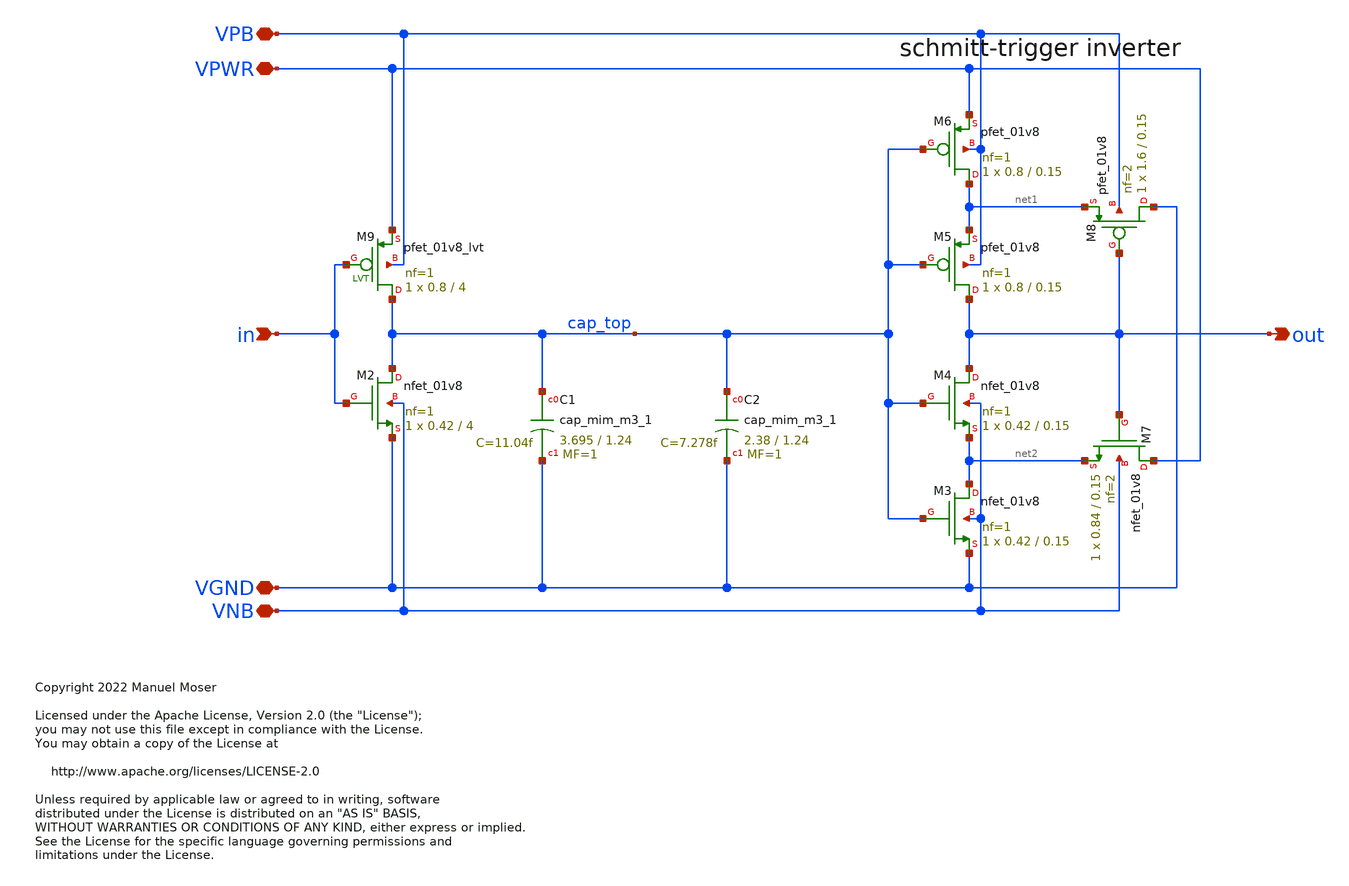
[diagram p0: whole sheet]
** sch_path: xschem/archive/sky130_mm_sc_hd_dlyMim5ns/sky130_mm_sc_hd_dlyMim5ns.sch
* Copyright 2022 Manuel Moser
* Licensed under the Apache License, Version 2.0 (the "License");
**.subckt sky130_mm_sc_hd_dlyMim5ns VPWR VGND in out VPB VNB
*.iopin VPWR
*.iopin VGND
*.ipin in
*.opin out
*.iopin VPB
*.iopin VNB
XM2 cap_top in VGND VNB sky130_fd_pr__nfet_01v8 L=4 W=0.42 nf=1 ad='int((nf+1)/2) * W/nf * 0.29' as='int((nf+2)/2) * W/nf * 0.29'
+ pd='2*int((nf+1)/2) * (W/nf + 0.29)' ps='2*int((nf+2)/2) * (W/nf + 0.29)' nrd='0.29 / W' nrs='0.29 / W'
+ sa=0 sb=0 sd=0 mult=1 m=1
XM3 net2 cap_top VGND VNB sky130_fd_pr__nfet_01v8 L=0.15 W=0.42 nf=1 ad='int((nf+1)/2) * W/nf * 0.29'
+ as='int((nf+2)/2) * W/nf * 0.29' pd='2*int((nf+1)/2) * (W/nf + 0.29)' ps='2*int((nf+2)/2) * (W/nf + 0.29)'
+ nrd='0.29 / W' nrs='0.29 / W' sa=0 sb=0 sd=0 mult=1 m=1
XM4 out cap_top net2 VNB sky130_fd_pr__nfet_01v8 L=0.15 W=0.42 nf=1 ad='int((nf+1)/2) * W/nf * 0.29'
+ as='int((nf+2)/2) * W/nf * 0.29' pd='2*int((nf+1)/2) * (W/nf + 0.29)' ps='2*int((nf+2)/2) * (W/nf + 0.29)'
+ nrd='0.29 / W' nrs='0.29 / W' sa=0 sb=0 sd=0 mult=1 m=1
XM5 out cap_top net1 VPB sky130_fd_pr__pfet_01v8 L=0.15 W=0.8 nf=1 ad='int((nf+1)/2) * W/nf * 0.29' as='int((nf+2)/2) * W/nf * 0.29'
+ pd='2*int((nf+1)/2) * (W/nf + 0.29)' ps='2*int((nf+2)/2) * (W/nf + 0.29)' nrd='0.29 / W' nrs='0.29 / W'
+ sa=0 sb=0 sd=0 mult=1 m=1
XM6 net1 cap_top VPWR VPB sky130_fd_pr__pfet_01v8 L=0.15 W=0.8 nf=1 ad='int((nf+1)/2) * W/nf * 0.29'
+ as='int((nf+2)/2) * W/nf * 0.29' pd='2*int((nf+1)/2) * (W/nf + 0.29)' ps='2*int((nf+2)/2) * (W/nf + 0.29)'
+ nrd='0.29 / W' nrs='0.29 / W' sa=0 sb=0 sd=0 mult=1 m=1
XM7 VPWR out net2 VNB sky130_fd_pr__nfet_01v8 L=0.15 W=0.84 nf=2 ad='int((nf+1)/2) * W/nf * 0.29' as='int((nf+2)/2) * W/nf * 0.29'
+ pd='2*int((nf+1)/2) * (W/nf + 0.29)' ps='2*int((nf+2)/2) * (W/nf + 0.29)' nrd='0.29 / W' nrs='0.29 / W'
+ sa=0 sb=0 sd=0 mult=1 m=1
XM8 VGND out net1 VPB sky130_fd_pr__pfet_01v8 L=0.15 W=1.6 nf=2 ad='int((nf+1)/2) * W/nf * 0.29' as='int((nf+2)/2) * W/nf * 0.29'
+ pd='2*int((nf+1)/2) * (W/nf + 0.29)' ps='2*int((nf+2)/2) * (W/nf + 0.29)' nrd='0.29 / W' nrs='0.29 / W'
+ sa=0 sb=0 sd=0 mult=1 m=1
XC1 cap_top VGND sky130_fd_pr__cap_mim_m3_1 W=3.695 L=1.24 MF=1 m=1
XC2 cap_top VGND sky130_fd_pr__cap_mim_m3_1 W=2.38 L=1.24 MF=1 m=1
XM9 cap_top in VPWR VPB sky130_fd_pr__pfet_01v8_lvt L=4 W=0.8 nf=1 ad='int((nf+1)/2) * W/nf * 0.29' as='int((nf+2)/2) * W/nf * 0.29'
+ pd='2*int((nf+1)/2) * (W/nf + 0.29)' ps='2*int((nf+2)/2) * (W/nf + 0.29)' nrd='0.29 / W' nrs='0.29 / W'
+ sa=0 sb=0 sd=0 mult=1 m=1
**.ends
.end
